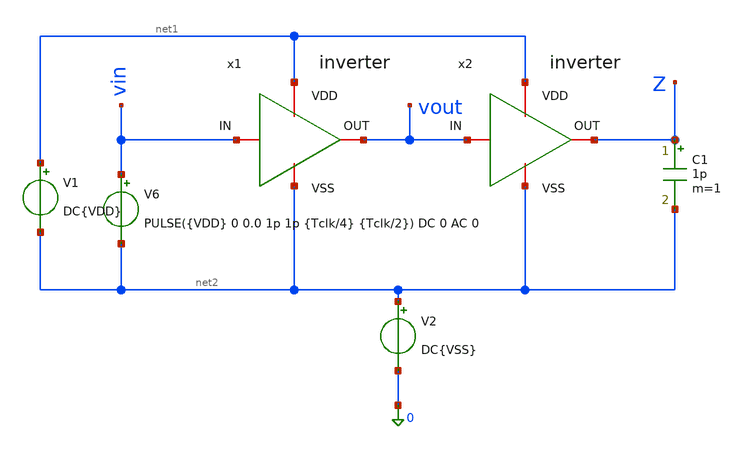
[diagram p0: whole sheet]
** sch_path: verification/testbenches/tb_inverter.sch
**.subckt tb_inverter
C1 Z net2 1p m=1
V1 net1 net2 DC{VDD}
V2 net2 0 DC{VSS}
V6 vin net2 PULSE({VDD} 0 0.0 1p 1p {Tclk/4} {Tclk/2}) DC 0 AC 0
x1 net1 vin vout net2 inverter
x2 net1 vout Z net2 inverter
**** begin user architecture code


* Circuit Parameters
.param VDD = 1.2
.param VSS = 0.0
.param Tclk = 10n
.options TEMP = 27.0
* Include Models - IHP SG13G2
.lib cornerMOSlv.lib mos_tt
* OP Parameters & Singals to save
.save all
*Simulations
.control
tran 0.01u 100n
setplot tran1
plot v(vin) v(vout)+1.2
reset
dc V6 0 1.2 0.01
setplot dc
plot vin vout ylabel vout xlabel vin
set filetype = ascii
write dcsweep.raw
.endc
.end


**** end user architecture code
**.ends

* expanding   symbol:  blocks/inverter/inverter.sym # of pins=4
** sym_path: blocks/inverter/inverter.sym
** sch_path: blocks/inverter/inverter.sch
.subckt inverter VDD IN OUT VSS
*.iopin VDD
*.iopin VSS
*.iopin OUT
*.iopin IN
XM1 OUT IN VSS VSS sg13_lv_nmos w=0.15u l=0.13u ng=1 m=1 mm_ok=1
XM2 OUT IN VDD VDD sg13_lv_pmos w=0.15u l=0.13u ng=1 m=1 mm_ok=1
.ends

.end
